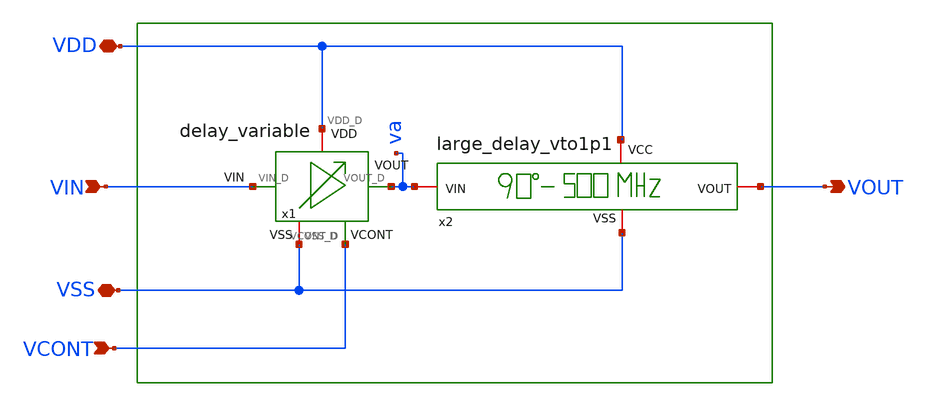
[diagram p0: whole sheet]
** sch_path: xschem/delay_variable_line/variable_delay_line.sch
* IHP-GmbH/IHP-Open-PDK/ihp-sg13g2/libs.tech/xschem/sg13g2_stdcells/sg13g2_dlygate4sd2_1.sch:
* Copyright 2023 IHP PDK Authors
* Licensed under the Apache License, Version 2.0 (the "License");
**.subckt variable_delay_line VSS VDD VIN VOUT VCONT
*.iopin VSS
*.iopin VDD
*.ipin VIN
*.opin VOUT
*.ipin VCONT
x1 VDD VIN va VCONT VSS delay_variable
x2 VDD VSS va VOUT large_delay_vto1p1
**.ends

* expanding   symbol:  /foss/designs/UNIC-CASS-Aug25/sch/delay_variable/delay_variable.sym # of
*+ pins=5
** sym_path: xschem/delay_variable/delay_variable.sym
** sch_path: xschem/delay_variable/delay_variable.sch
.subckt delay_variable VDD_D VIN_D VOUT_D VCONT_D VSS_D
*.iopin VSS_D
*.iopin VDD_D
*.opin VOUT_D
*.ipin VCONT_D
*.ipin VIN_D
XM3 net3 VCONT_D VSS_D VSS_D sg13_lv_nmos w=1u l=0.13u ng=1 m=1 mm_ok=1
XM5 net2 VCONT_D VSS_D VSS_D sg13_lv_nmos w=2u l=2u ng=1 m=1 mm_ok=1
XM4 net3 net3 VDD_D VDD_D sg13_lv_pmos w=2.24u l=0.13u ng=1 m=1 mm_ok=1
XM6 net1 net3 VDD_D VDD_D sg13_lv_pmos w=4u l=2u ng=1 m=1 mm_ok=1
XM7 VOUT_D VIN_D net1 VDD_D sg13_lv_pmos w=20u l=2u ng=4 m=1 mm_ok=1
XM8 VOUT_D VIN_D net2 VSS_D sg13_lv_nmos w=5u l=3u ng=1 m=1 mm_ok=1
.ends


* expanding   symbol:  /foss/designs/UNIC-CASS-Aug25/sch/large_delay_vto1p1/large_delay_vto1p1.sym #
*+ of pins=4
** sym_path: xschem/large_delay_vto1p1/large_delay_vto1p1.sym
** sch_path: xschem/large_delay_vto1p1/large_delay_vto1p1.sch
.subckt large_delay_vto1p1 VCC VSS VIN VOUT
*.iopin VIN
*.iopin VOUT
*.iopin VCC
*.iopin VSS
x1 VOUT VIN VCC VSS sg13g2_dlygate4sd2_1
x2 VOUT VIN VCC VSS sg13g2_dlygate4sd2_1
x3 VOUT VIN VCC VSS sg13g2_dlygate4sd2_1
x10 VOUT VIN VCC VSS sg13g2_dlygate4sd2_1
.ends


* expanding   symbol:  sg13g2_stdcells/sg13g2_dlygate4sd3_1.sym # of pins=2
** sym_path: sg13g2_stdcells/sg13g2_dlygate4sd3_1.sym
** sch_path: sg13g2_stdcells/sg13g2_dlygate4sd3_1.sch
.subckt sg13g2_dlygate4sd3_1 X A VDD VSS
*.ipin A
*.opin X
*.iopin VDD
*.iopin VSS
XM1 net3 A VSS VSS sg13_lv_nmos w=420.00n l=130.00n ng=1 m=1 mm_ok=1
XM2 net1 net3 VSS VSS sg13_lv_nmos w=420.00n l=500.0n ng=1 m=1 mm_ok=1
XM3 net2 net1 VSS VSS sg13_lv_nmos w=420.00n l=500.0n ng=1 m=1 mm_ok=1
XM4 X net2 VSS VSS sg13_lv_nmos w=740.00n l=130.00n ng=1 m=1 mm_ok=1
XM5 net3 A VDD VDD sg13_lv_pmos w=420.00n l=130.00n ng=1 m=1 mm_ok=1
XM6 net1 net3 VDD VDD sg13_lv_pmos w=1.000u l=500.0n ng=1 m=1 mm_ok=1
XM7 net2 net1 VDD VDD sg13_lv_pmos w=1.000u l=500.0n ng=1 m=1 mm_ok=1
XM8 X net2 VDD VDD sg13_lv_pmos w=1.12u l=130.00n ng=1 m=1 mm_ok=1
.ends


* expanding   symbol:  sg13g2_stdcells/sg13g2_dlygate4sd2_1.sym # of pins=2
** sym_path: sg13g2_stdcells/sg13g2_dlygate4sd2_1.sym
** sch_path: sg13g2_stdcells/sg13g2_dlygate4sd2_1.sch
.subckt sg13g2_dlygate4sd2_1 X A VDD VSS
*.ipin A
*.opin X
*.iopin VDD
*.iopin VSS
XM1 net2 A VSS VSS sg13_lv_nmos w=420.00n l=130.00n ng=1 m=1 mm_ok=1
XM2 net1 net2 VSS VSS sg13_lv_nmos w=420.00n l=180.00n ng=1 m=1 mm_ok=1
XM3 net3 net1 VSS VSS sg13_lv_nmos w=420.00n l=180.00n ng=1 m=1 mm_ok=1
XM4 X net3 VSS VSS sg13_lv_nmos w=740.00n l=130.00n ng=1 m=1 mm_ok=1
XM5 net2 A VDD VDD sg13_lv_pmos w=420.00n l=130.00n ng=1 m=1 mm_ok=1
XM6 net1 net2 VDD VDD sg13_lv_pmos w=1.000u l=250.00n ng=1 m=1 mm_ok=1
XM7 net3 net1 VDD VDD sg13_lv_pmos w=1.000u l=250.00n ng=1 m=1 mm_ok=1
XM8 X net3 VDD VDD sg13_lv_pmos w=1.12u l=130.00n ng=1 m=1 mm_ok=1
.ends

.end
